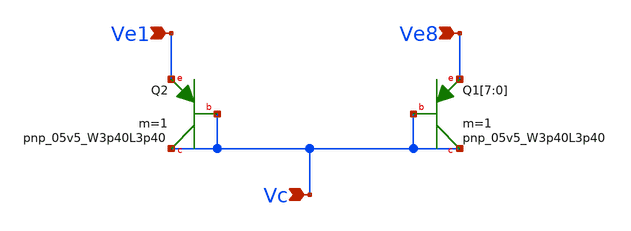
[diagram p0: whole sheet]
** sch_path: design/LELO_GR01_SKY130A/Diodes.sch
**.subckt Diodes Ve1 Ve8 Vc
*.ipin Ve1
*.ipin Ve8
*.ipin Vc
XQ1[7] Vc Vc Ve8 sky130_fd_pr__pnp_05v5_W3p40L3p40 m=1
XQ1[6] Vc Vc Ve8 sky130_fd_pr__pnp_05v5_W3p40L3p40 m=1
XQ1[5] Vc Vc Ve8 sky130_fd_pr__pnp_05v5_W3p40L3p40 m=1
XQ1[4] Vc Vc Ve8 sky130_fd_pr__pnp_05v5_W3p40L3p40 m=1
XQ1[3] Vc Vc Ve8 sky130_fd_pr__pnp_05v5_W3p40L3p40 m=1
XQ1[2] Vc Vc Ve8 sky130_fd_pr__pnp_05v5_W3p40L3p40 m=1
XQ1[1] Vc Vc Ve8 sky130_fd_pr__pnp_05v5_W3p40L3p40 m=1
XQ1[0] Vc Vc Ve8 sky130_fd_pr__pnp_05v5_W3p40L3p40 m=1
XQ2 Vc Vc Ve1 sky130_fd_pr__pnp_05v5_W3p40L3p40 m=1
**.ends
.end
